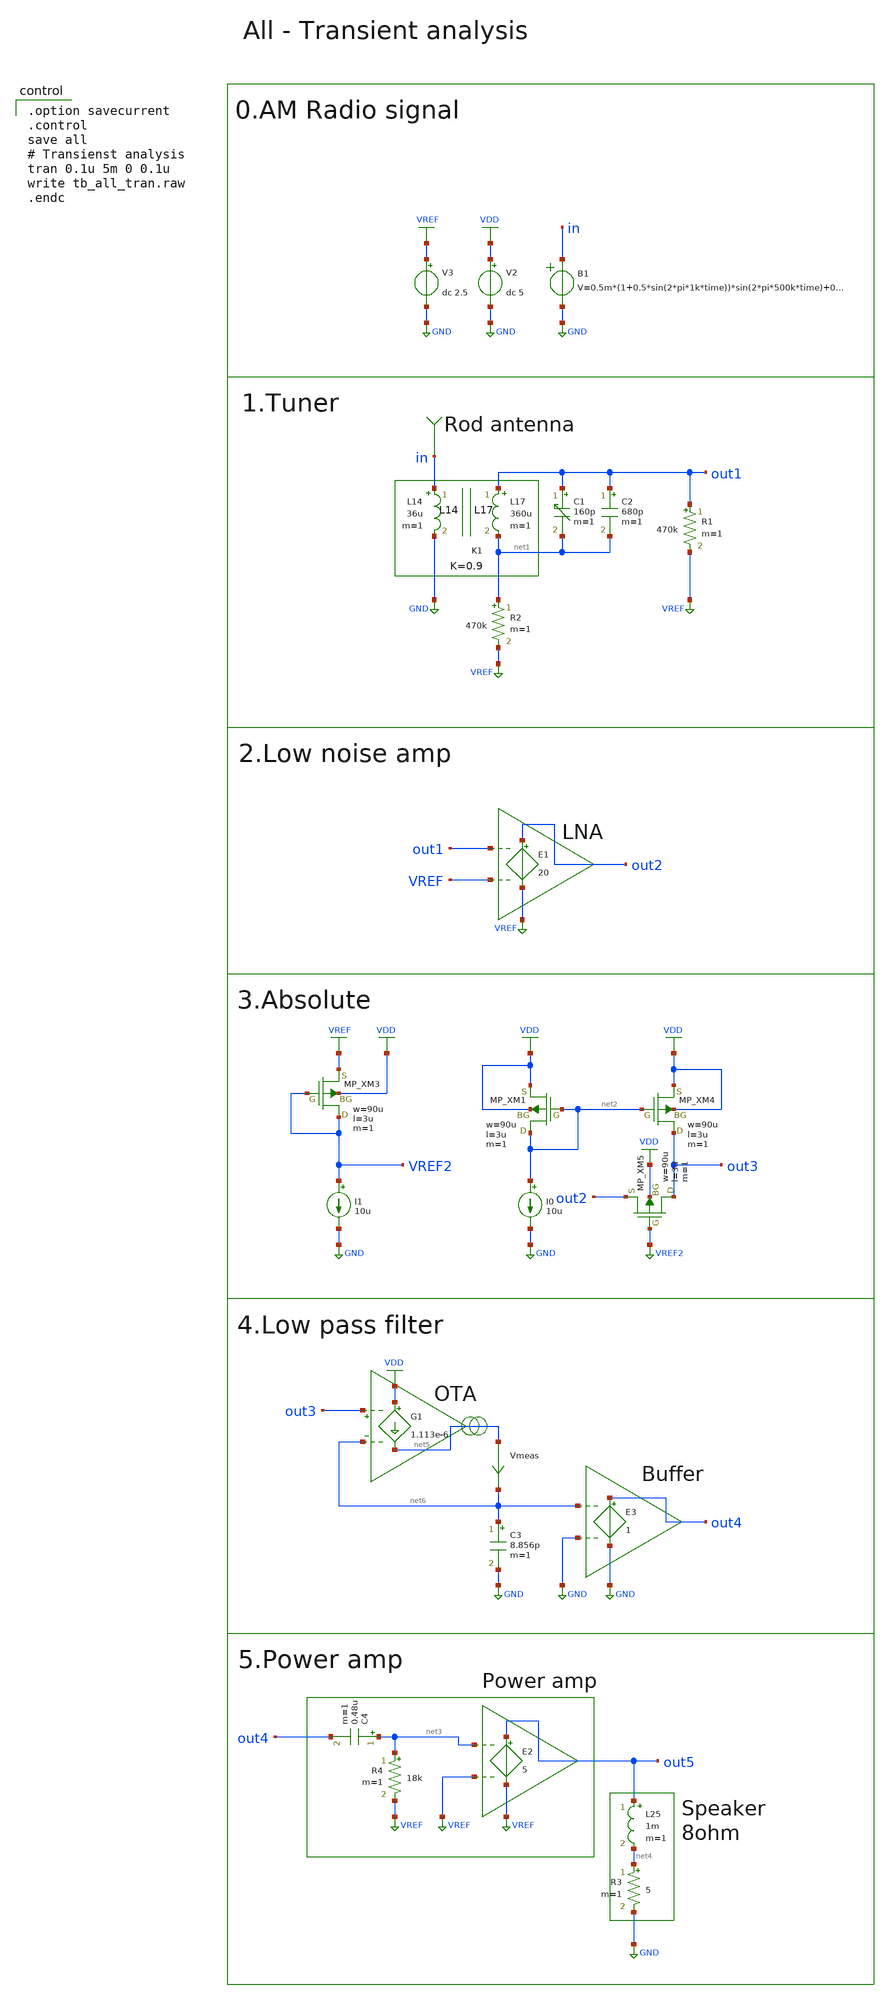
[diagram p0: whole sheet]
** sch_path: member_project/AM_Radio/Yamada3/xschem/tb_all_tran.sch
**.subckt tb_all_tran
V2 VDD GND dc 5
V3 VREF GND dc 2.5
B1 in GND
+ V=0.5m*(1+0.5*sin(2*pi*1k*time))*sin(2*pi*500k*time)+0.5m*(1+0.5*sin(2*pi*3k*time))*sin(2*pi*800k*time)+0.5m*(1+0.5*sin(2*pi*5k*time))*sin(2*pi*663.74k*time)
C1 out1 net1 160p m=1
L14 in GND 36u m=1
K1 L17 L14 0.9
L17 out1 net1 360u m=1
R1 out1 VREF 470k m=1
R2 net1 VREF 470k m=1
C2 out1 net1 680p m=1
I0 net2 GND 10u
I1 VREF2 GND 10u
XM3 VREF2 VREF2 VREF VDD PMOS w=90u l=3u as=0 ad=0 ps=0 pd=0 nrd=0 nrs=0 m=1
XM1 net2 net2 VDD VDD PMOS w=90u l=3u as=0 ad=0 ps=0 pd=0 nrd=0 nrs=0 m=1
XM4 out3 net2 VDD VDD PMOS w=90u l=3u as=0 ad=0 ps=0 pd=0 nrd=0 nrs=0 m=1
XM5 out3 VREF2 out2 VDD PMOS w=90u l=3u as=0 ad=0 ps=0 pd=0 nrd=0 nrs=0 m=1
E1 out2 VREF out1 VREF 20
E2 out5 VREF net3 VREF 5
C4 net3 out4 0.48u m=1
R3 net4 GND 5 m=1
R4 net3 VREF 18k m=1
L25 out5 net4 1m m=1
G1 VDD net5 out3 net6 1.113e-6
Vmeas net5 net6 0
.save i(vmeas)
C3 net6 GND 8.856p m=1
E3 out4 GND net6 GND 1
**** begin user architecture code

.option savecurrent
.control
save all
# Transienst analysis
tran 0.1u 5m 0 0.1u
write tb_all_tran.raw
.endc

 .include $::LIB/ip62_models
**** end user architecture code
**.ends
.GLOBAL GND
.GLOBAL VDD
.GLOBAL VREF
.GLOBAL VREF2
.end
